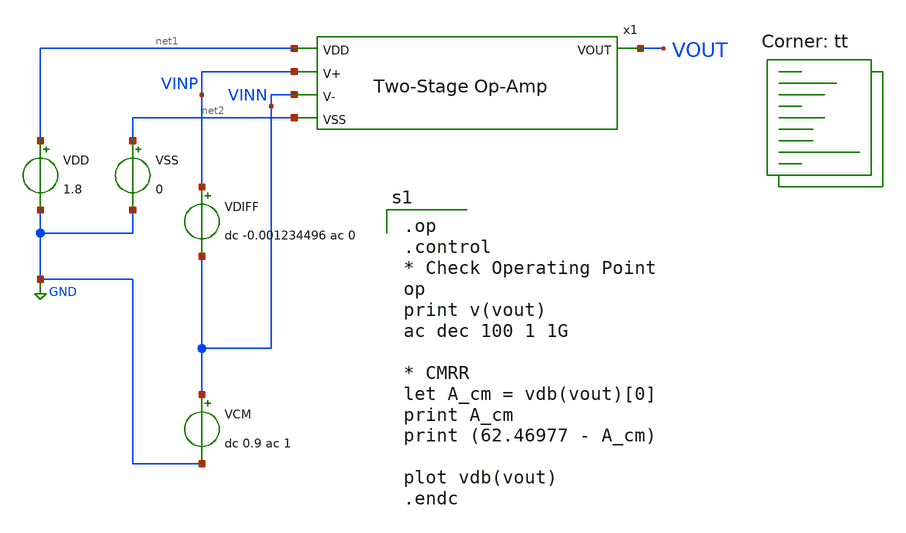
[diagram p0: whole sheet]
** sch_path: analog/schematics/tb_cmrr.sch
**.subckt tb_cmrr
VDD net1 GND 1.8
VSS net2 GND 0
VCM VINN GND dc 0.9 ac 1
x1 net1 VINP VINN VOUT net2 bootcamp_opamp
VDIFF VINP VINN dc -0.001234496 ac 0
**** begin user architecture code

.op
.control
* Check Operating Point
op
print v(vout)
ac dec 100 1 1G

* CMRR
let A_cm = vdb(vout)[0]
print A_cm
print (62.46977 - A_cm)

plot vdb(vout)
.endc

.lib $::SKYWATER_MODELS/sky130.lib.spice tt
**** end user architecture code
**.ends

* expanding   symbol:  bootcamp_opamp.sym # of pins=5
** sym_path: analog/schematics/bootcamp_opamp.sym
** sch_path: analog/schematics/bootcamp_opamp.sch
.subckt bootcamp_opamp VDD V+ V- VOUT VSS
*.ipin V+
*.ipin V-
*.opin VOUT
*.ipin VDD
*.ipin VSS
XM1 net1 V+ net3 VSS sky130_fd_pr__nfet_01v8 L=1 W=4 nf=1 ad='int((nf+1)/2) * W/nf * 0.29' as='int((nf+2)/2) * W/nf * 0.29'
+ pd='2*int((nf+1)/2) * (W/nf + 0.29)' ps='2*int((nf+2)/2) * (W/nf + 0.29)' nrd='0.29 / W' nrs='0.29 / W'
+ sa=0 sb=0 sd=0 mult=1 m=1
XM2 net2 V- net3 VSS sky130_fd_pr__nfet_01v8 L=1 W=4 nf=1 ad='int((nf+1)/2) * W/nf * 0.29' as='int((nf+2)/2) * W/nf * 0.29'
+ pd='2*int((nf+1)/2) * (W/nf + 0.29)' ps='2*int((nf+2)/2) * (W/nf + 0.29)' nrd='0.29 / W' nrs='0.29 / W'
+ sa=0 sb=0 sd=0 mult=1 m=1
XM3 net1 net1 VDD VDD sky130_fd_pr__pfet_01v8 L=1 W=4 nf=1 ad='int((nf+1)/2) * W/nf * 0.29' as='int((nf+2)/2) * W/nf * 0.29'
+ pd='2*int((nf+1)/2) * (W/nf + 0.29)' ps='2*int((nf+2)/2) * (W/nf + 0.29)' nrd='0.29 / W' nrs='0.29 / W'
+ sa=0 sb=0 sd=0 mult=1 m=1
XM4 net2 net1 VDD VDD sky130_fd_pr__pfet_01v8 L=1 W=4 nf=1 ad='int((nf+1)/2) * W/nf * 0.29' as='int((nf+2)/2) * W/nf * 0.29'
+ pd='2*int((nf+1)/2) * (W/nf + 0.29)' ps='2*int((nf+2)/2) * (W/nf + 0.29)' nrd='0.29 / W' nrs='0.29 / W'
+ sa=0 sb=0 sd=0 mult=1 m=1
XM5 net3 net4 VSS VSS sky130_fd_pr__nfet_01v8 L=2 W=4 nf=1 ad='int((nf+1)/2) * W/nf * 0.29' as='int((nf+2)/2) * W/nf * 0.29'
+ pd='2*int((nf+1)/2) * (W/nf + 0.29)' ps='2*int((nf+2)/2) * (W/nf + 0.29)' nrd='0.29 / W' nrs='0.29 / W'
+ sa=0 sb=0 sd=0 mult=1 m=1
XM6 net4 net4 VSS VSS sky130_fd_pr__nfet_01v8 L=2 W=4 nf=1 ad='int((nf+1)/2) * W/nf * 0.29' as='int((nf+2)/2) * W/nf * 0.29'
+ pd='2*int((nf+1)/2) * (W/nf + 0.29)' ps='2*int((nf+2)/2) * (W/nf + 0.29)' nrd='0.29 / W' nrs='0.29 / W'
+ sa=0 sb=0 sd=0 mult=1 m=1
XM8 VOUT net4 VSS VSS sky130_fd_pr__nfet_01v8 L=0.5 W=2 nf=1 ad='int((nf+1)/2) * W/nf * 0.29' as='int((nf+2)/2) * W/nf * 0.29'
+ pd='2*int((nf+1)/2) * (W/nf + 0.29)' ps='2*int((nf+2)/2) * (W/nf + 0.29)' nrd='0.29 / W' nrs='0.29 / W'
+ sa=0 sb=0 sd=0 mult=1 m=1
XC1 net2 VOUT sky130_fd_pr__cap_mim_m3_1 W=22 L=22 MF=1 m=1
R1 VDD net4 12k m=1
XM7 VOUT net2 VDD VDD sky130_fd_pr__pfet_01v8 L=0.5 W=8 nf=1 ad='int((nf+1)/2) * W/nf * 0.29' as='int((nf+2)/2) * W/nf * 0.29'
+ pd='2*int((nf+1)/2) * (W/nf + 0.29)' ps='2*int((nf+2)/2) * (W/nf + 0.29)' nrd='0.29 / W' nrs='0.29 / W'
+ sa=0 sb=0 sd=0 mult=1 m=1
.ends

.GLOBAL GND
.end
